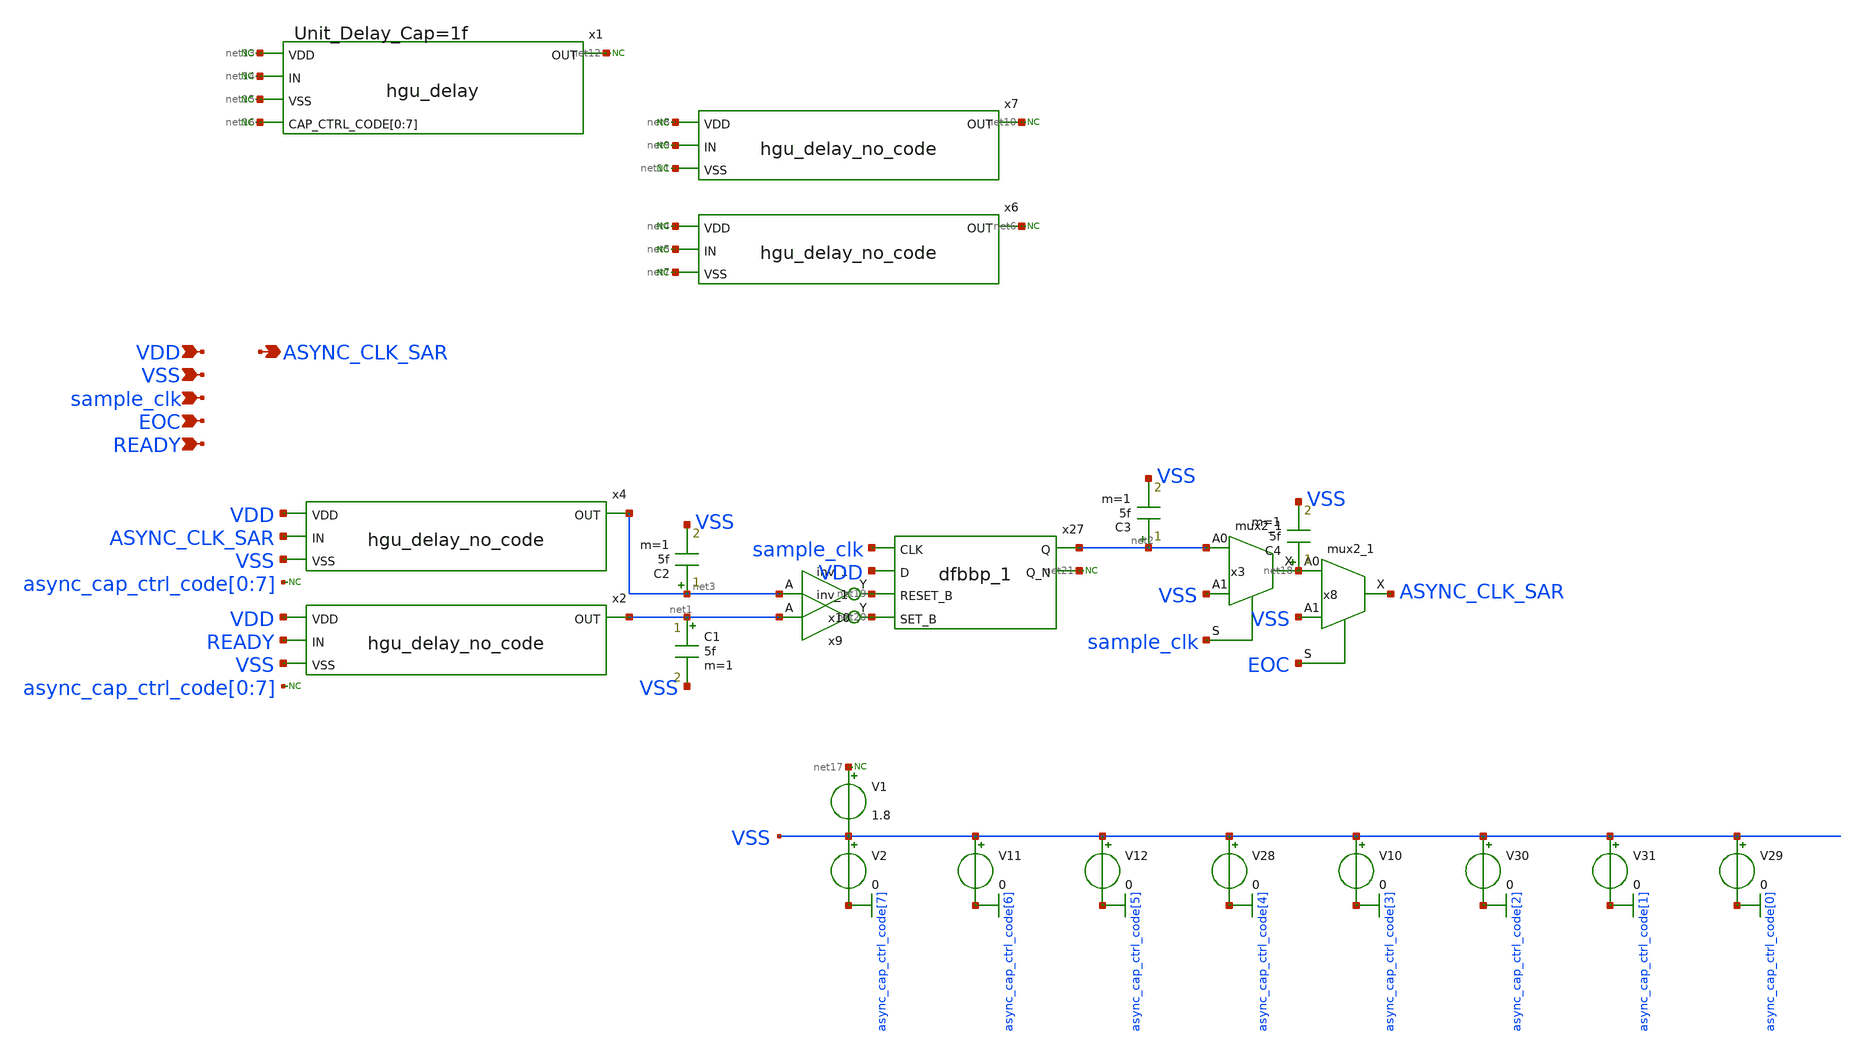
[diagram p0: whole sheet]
** sch_path: hgu/xschem/hgu_clk_async.sch
**.subckt hgu_clk_async VDD ASYNC_CLK_SAR VSS sample_clk EOC READY
*.ipin VDD
*.opin ASYNC_CLK_SAR
*.ipin VSS
*.ipin sample_clk
*.ipin EOC
*.ipin READY
V10 VSS async_cap_ctrl_code[3] 0
V11 VSS async_cap_ctrl_code[6] 0
V12 VSS async_cap_ctrl_code[5] 0
V28 VSS async_cap_ctrl_code[4] 0
V29 VSS async_cap_ctrl_code[0] 0
V30 VSS async_cap_ctrl_code[2] 0
V31 VSS async_cap_ctrl_code[1] 0
x6 net4 net5 net6 net7 hgu_delay_no_code
x7 net8 net9 net10 net11 hgu_delay_no_code
* noconn #net12
* noconn #net13
* noconn #net14
* noconn #net15
* noconn #net16
V1 net17 VSS 1.8
x3 net2 VSS sample_clk VGND VNB VPB VPWR net18 sky130_fd_sc_hd__mux2_1
x8 net18 VSS EOC VGND VNB VPB VPWR ASYNC_CLK_SAR sky130_fd_sc_hd__mux2_1
x27 sample_clk VDD net19 net20 VGND VNB VPB VPWR net2 net21 sky130_fd_sc_hd__dfbbp_1
x9 net1 VGND VNB VPB VPWR net20 sky130_fd_sc_hd__inv_1
x10 net3 VGND VNB VPB VPWR net19 sky130_fd_sc_hd__inv_1
* noconn #net21
C1 net1 VSS 5f m=1
C2 net3 VSS 5f m=1
C3 net2 VSS 5f m=1
C4 net18 VSS 5f m=1
x1 net13 net14 net12 net15 net16 net16 net16 net16 net16 net16 net16 net16 hgu_delay DELAY_CAP=1f
* noconn #net8
* noconn #net9
* noconn #net11
* noconn #net4
* noconn #net5
* noconn #net7
* noconn #net10
* noconn #net6
V2 VSS async_cap_ctrl_code[7] 0
* noconn #net17
x2 VDD READY net1 VSS hgu_delay_no_code
x4 VDD ASYNC_CLK_SAR net3 VSS hgu_delay_no_code
* noconn async_cap_ctrl_code[0:7]
* noconn async_cap_ctrl_code[0:7]
**.ends
.GLOBAL async_cap_ctrl_code[7]
.GLOBAL async_cap_ctrl_code[6]
.GLOBAL async_cap_ctrl_code[5]
.GLOBAL async_cap_ctrl_code[4]
.GLOBAL async_cap_ctrl_code[3]
.GLOBAL async_cap_ctrl_code[2]
.GLOBAL async_cap_ctrl_code[1]
.GLOBAL async_cap_ctrl_code[0]
.end
